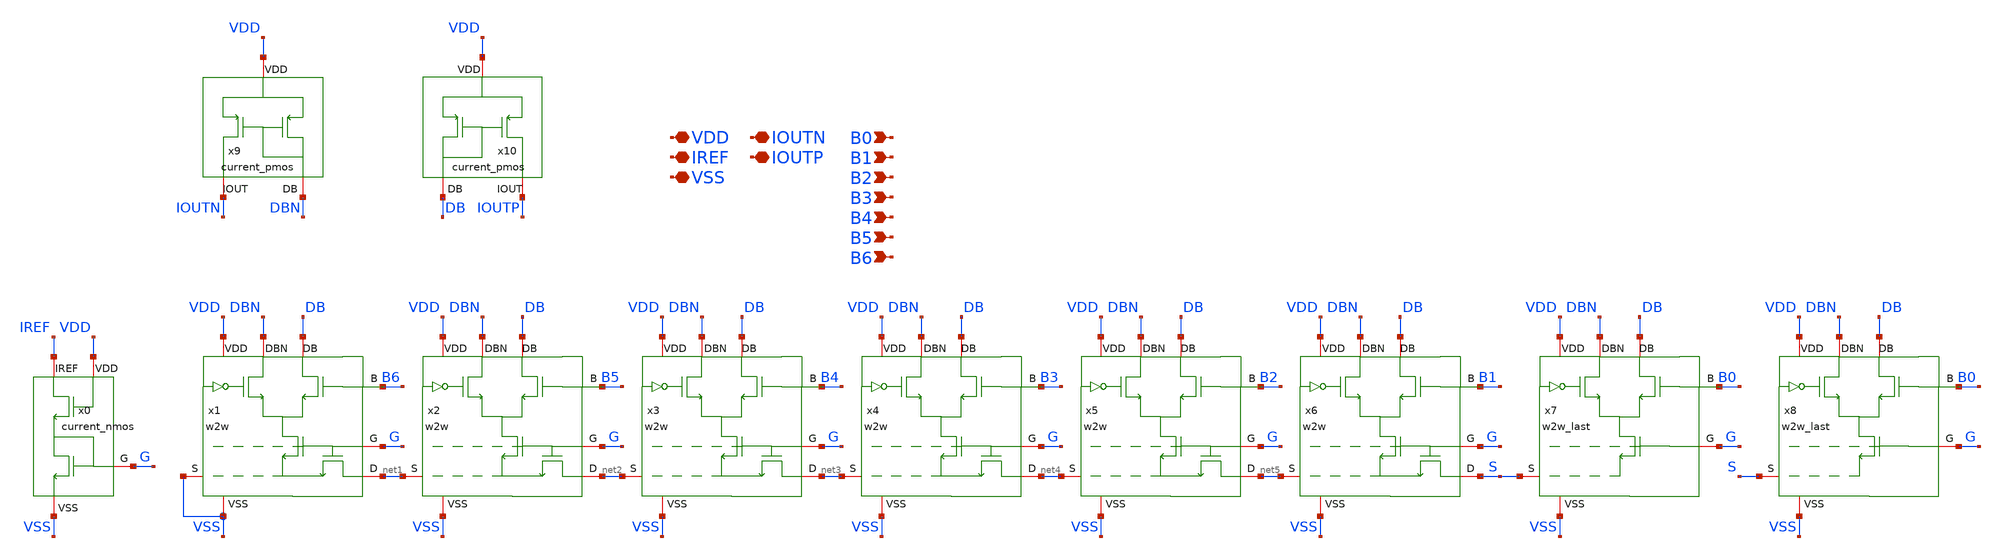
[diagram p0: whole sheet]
** sch_path: W2WDAC/W2W-DAC/W2W_BOX/w2w_top.sch
**.subckt w2w_top VSS IREF VDD IOUTN IOUTP B0 B1 B2 B3 B4 B5 B6
*.iopin VSS
*.iopin IREF
*.iopin VDD
*.iopin IOUTN
*.iopin IOUTP
*.ipin B0
*.ipin B1
*.ipin B2
*.ipin B3
*.ipin B4
*.ipin B5
*.ipin B6
x1 DBN DB VDD B6 VSS G net1 VSS w2w
x2 DBN DB VDD B5 VSS G net2 net1 w2w
x3 DBN DB VDD B4 VSS G net3 net2 w2w
x4 DBN DB VDD B3 VSS G net4 net3 w2w
x5 DBN DB VDD B2 VSS G net5 net4 w2w
x6 DBN DB VDD B1 VSS G S net5 w2w
x0 IREF VDD G VSS current_nmos
x9 VDD IOUTN DBN current_pmos
x10 VDD IOUTP DB current_pmos
x7 DBN DB VDD B0 VSS G S w2w_last
x8 DBN DB VDD B0 VSS G S w2w_last
**.ends
.end
